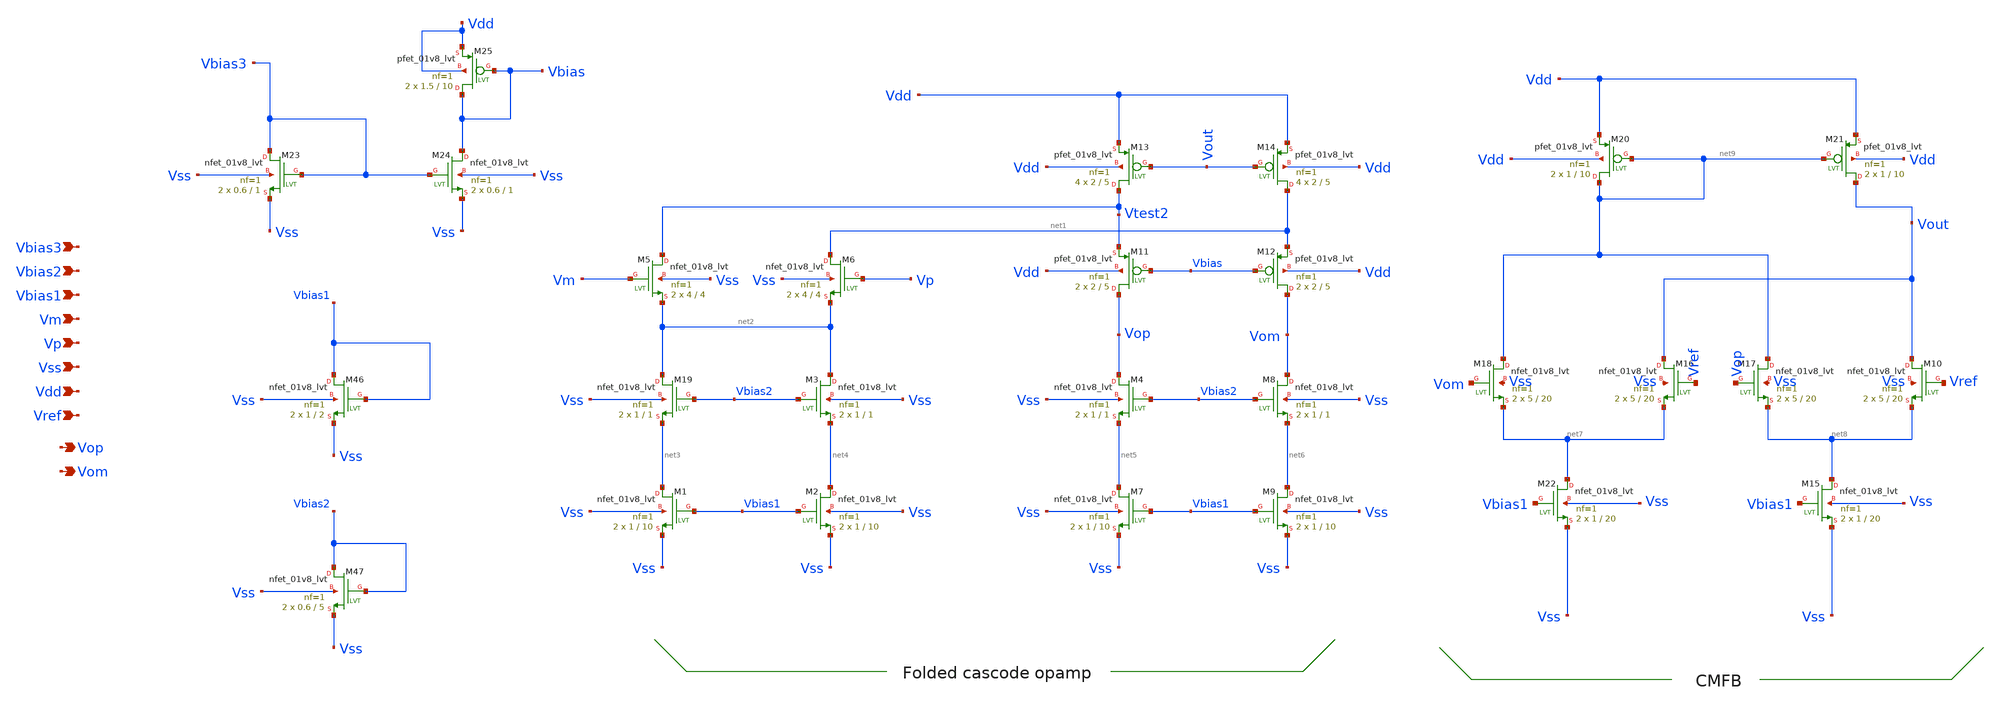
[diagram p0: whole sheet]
** sch_path: src/Opamp_Design/src/Diff_opamp.sch
**.subckt Diff_opamp Vss Vop Vdd Vp Vm Vref Vom Vbias1 Vbias2 Vbias3
*.ipin Vss
*.opin Vop
*.ipin Vdd
*.ipin Vp
*.ipin Vm
*.ipin Vref
*.opin Vom
*.ipin Vbias1
*.ipin Vbias2
*.ipin Vbias3
XM5 Vtest2 Vm net2 Vss sky130_fd_pr__nfet_01v8_lvt L=4 W=4 nf=1 ad='int((nf+1)/2) * W/nf * 0.29' as='int((nf+2)/2) * W/nf * 0.29'
+ pd='2*int((nf+1)/2) * (W/nf + 0.29)' ps='2*int((nf+2)/2) * (W/nf + 0.29)' nrd='0.29 / W' nrs='0.29 / W'
+ sa=0 sb=0 sd=0 mult=2 m=2
XM6 net1 Vp net2 Vss sky130_fd_pr__nfet_01v8_lvt L=4 W=4 nf=1 ad='int((nf+1)/2) * W/nf * 0.29' as='int((nf+2)/2) * W/nf * 0.29'
+ pd='2*int((nf+1)/2) * (W/nf + 0.29)' ps='2*int((nf+2)/2) * (W/nf + 0.29)' nrd='0.29 / W' nrs='0.29 / W'
+ sa=0 sb=0 sd=0 mult=2 m=2
XM11 Vop Vbias Vtest2 Vdd sky130_fd_pr__pfet_01v8_lvt L=5 W=2 nf=1 ad='int((nf+1)/2) * W/nf * 0.29' as='int((nf+2)/2) * W/nf * 0.29'
+ pd='2*int((nf+1)/2) * (W/nf + 0.29)' ps='2*int((nf+2)/2) * (W/nf + 0.29)' nrd='0.29 / W' nrs='0.29 / W'
+ sa=0 sb=0 sd=0 mult=2 m=2
XM12 Vom Vbias net1 Vdd sky130_fd_pr__pfet_01v8_lvt L=5 W=2 nf=1 ad='int((nf+1)/2) * W/nf * 0.29' as='int((nf+2)/2) * W/nf * 0.29'
+ pd='2*int((nf+1)/2) * (W/nf + 0.29)' ps='2*int((nf+2)/2) * (W/nf + 0.29)' nrd='0.29 / W' nrs='0.29 / W'
+ sa=0 sb=0 sd=0 mult=2 m=2
XM13 Vtest2 Vout Vdd Vdd sky130_fd_pr__pfet_01v8_lvt L=5 W=2 nf=1 ad='int((nf+1)/2) * W/nf * 0.29' as='int((nf+2)/2) * W/nf * 0.29'
+ pd='2*int((nf+1)/2) * (W/nf + 0.29)' ps='2*int((nf+2)/2) * (W/nf + 0.29)' nrd='0.29 / W' nrs='0.29 / W'
+ sa=0 sb=0 sd=0 mult=4 m=4
XM14 net1 Vout Vdd Vdd sky130_fd_pr__pfet_01v8_lvt L=5 W=2 nf=1 ad='int((nf+1)/2) * W/nf * 0.29' as='int((nf+2)/2) * W/nf * 0.29'
+ pd='2*int((nf+1)/2) * (W/nf + 0.29)' ps='2*int((nf+2)/2) * (W/nf + 0.29)' nrd='0.29 / W' nrs='0.29 / W'
+ sa=0 sb=0 sd=0 mult=4 m=4
XM19 net2 Vbias2 net3 Vss sky130_fd_pr__nfet_01v8_lvt L=1 W=1 nf=1 ad='int((nf+1)/2) * W/nf * 0.29' as='int((nf+2)/2) * W/nf * 0.29'
+ pd='2*int((nf+1)/2) * (W/nf + 0.29)' ps='2*int((nf+2)/2) * (W/nf + 0.29)' nrd='0.29 / W' nrs='0.29 / W'
+ sa=0 sb=0 sd=0 mult=2 m=2
XM1 net3 Vbias1 Vss Vss sky130_fd_pr__nfet_01v8_lvt L=10 W=1 nf=1 ad='int((nf+1)/2) * W/nf * 0.29' as='int((nf+2)/2) * W/nf * 0.29'
+ pd='2*int((nf+1)/2) * (W/nf + 0.29)' ps='2*int((nf+2)/2) * (W/nf + 0.29)' nrd='0.29 / W' nrs='0.29 / W'
+ sa=0 sb=0 sd=0 mult=2 m=2
XM2 net4 Vbias1 Vss Vss sky130_fd_pr__nfet_01v8_lvt L=10 W=1 nf=1 ad='int((nf+1)/2) * W/nf * 0.29' as='int((nf+2)/2) * W/nf * 0.29'
+ pd='2*int((nf+1)/2) * (W/nf + 0.29)' ps='2*int((nf+2)/2) * (W/nf + 0.29)' nrd='0.29 / W' nrs='0.29 / W'
+ sa=0 sb=0 sd=0 mult=2 m=2
XM3 net2 Vbias2 net4 Vss sky130_fd_pr__nfet_01v8_lvt L=1 W=1 nf=1 ad='int((nf+1)/2) * W/nf * 0.29' as='int((nf+2)/2) * W/nf * 0.29'
+ pd='2*int((nf+1)/2) * (W/nf + 0.29)' ps='2*int((nf+2)/2) * (W/nf + 0.29)' nrd='0.29 / W' nrs='0.29 / W'
+ sa=0 sb=0 sd=0 mult=2 m=2
XM4 Vop Vbias2 net5 Vss sky130_fd_pr__nfet_01v8_lvt L=1 W=1 nf=1 ad='int((nf+1)/2) * W/nf * 0.29' as='int((nf+2)/2) * W/nf * 0.29'
+ pd='2*int((nf+1)/2) * (W/nf + 0.29)' ps='2*int((nf+2)/2) * (W/nf + 0.29)' nrd='0.29 / W' nrs='0.29 / W'
+ sa=0 sb=0 sd=0 mult=2 m=2
XM7 net5 Vbias1 Vss Vss sky130_fd_pr__nfet_01v8_lvt L=10 W=1 nf=1 ad='int((nf+1)/2) * W/nf * 0.29' as='int((nf+2)/2) * W/nf * 0.29'
+ pd='2*int((nf+1)/2) * (W/nf + 0.29)' ps='2*int((nf+2)/2) * (W/nf + 0.29)' nrd='0.29 / W' nrs='0.29 / W'
+ sa=0 sb=0 sd=0 mult=2 m=2
XM8 Vom Vbias2 net6 Vss sky130_fd_pr__nfet_01v8_lvt L=1 W=1 nf=1 ad='int((nf+1)/2) * W/nf * 0.29' as='int((nf+2)/2) * W/nf * 0.29'
+ pd='2*int((nf+1)/2) * (W/nf + 0.29)' ps='2*int((nf+2)/2) * (W/nf + 0.29)' nrd='0.29 / W' nrs='0.29 / W'
+ sa=0 sb=0 sd=0 mult=2 m=2
XM9 net6 Vbias1 Vss Vss sky130_fd_pr__nfet_01v8_lvt L=10 W=1 nf=1 ad='int((nf+1)/2) * W/nf * 0.29' as='int((nf+2)/2) * W/nf * 0.29'
+ pd='2*int((nf+1)/2) * (W/nf + 0.29)' ps='2*int((nf+2)/2) * (W/nf + 0.29)' nrd='0.29 / W' nrs='0.29 / W'
+ sa=0 sb=0 sd=0 mult=2 m=2
XM10 Vout Vref net8 Vss sky130_fd_pr__nfet_01v8_lvt L=20 W=5 nf=1 ad='int((nf+1)/2) * W/nf * 0.29' as='int((nf+2)/2) * W/nf * 0.29'
+ pd='2*int((nf+1)/2) * (W/nf + 0.29)' ps='2*int((nf+2)/2) * (W/nf + 0.29)' nrd='0.29 / W' nrs='0.29 / W'
+ sa=0 sb=0 sd=0 mult=2 m=2
XM17 net9 Vop net8 Vss sky130_fd_pr__nfet_01v8_lvt L=20 W=5 nf=1 ad='int((nf+1)/2) * W/nf * 0.29' as='int((nf+2)/2) * W/nf * 0.29'
+ pd='2*int((nf+1)/2) * (W/nf + 0.29)' ps='2*int((nf+2)/2) * (W/nf + 0.29)' nrd='0.29 / W' nrs='0.29 / W'
+ sa=0 sb=0 sd=0 mult=2 m=2
XM18 net9 Vom net7 Vss sky130_fd_pr__nfet_01v8_lvt L=20 W=5 nf=1 ad='int((nf+1)/2) * W/nf * 0.29' as='int((nf+2)/2) * W/nf * 0.29'
+ pd='2*int((nf+1)/2) * (W/nf + 0.29)' ps='2*int((nf+2)/2) * (W/nf + 0.29)' nrd='0.29 / W' nrs='0.29 / W'
+ sa=0 sb=0 sd=0 mult=2 m=2
XM22 net7 Vbias1 Vss Vss sky130_fd_pr__nfet_01v8_lvt L=20 W=1 nf=1 ad='int((nf+1)/2) * W/nf * 0.29' as='int((nf+2)/2) * W/nf * 0.29'
+ pd='2*int((nf+1)/2) * (W/nf + 0.29)' ps='2*int((nf+2)/2) * (W/nf + 0.29)' nrd='0.29 / W' nrs='0.29 / W'
+ sa=0 sb=0 sd=0 mult=2 m=2
XM20 net9 net9 Vdd Vdd sky130_fd_pr__pfet_01v8_lvt L=10 W=1 nf=1 ad='int((nf+1)/2) * W/nf * 0.29' as='int((nf+2)/2) * W/nf * 0.29'
+ pd='2*int((nf+1)/2) * (W/nf + 0.29)' ps='2*int((nf+2)/2) * (W/nf + 0.29)' nrd='0.29 / W' nrs='0.29 / W'
+ sa=0 sb=0 sd=0 mult=2 m=2
XM21 Vout net9 Vdd Vdd sky130_fd_pr__pfet_01v8_lvt L=10 W=1 nf=1 ad='int((nf+1)/2) * W/nf * 0.29' as='int((nf+2)/2) * W/nf * 0.29'
+ pd='2*int((nf+1)/2) * (W/nf + 0.29)' ps='2*int((nf+2)/2) * (W/nf + 0.29)' nrd='0.29 / W' nrs='0.29 / W'
+ sa=0 sb=0 sd=0 mult=2 m=2
XM15 net8 Vbias1 Vss Vss sky130_fd_pr__nfet_01v8_lvt L=20 W=1 nf=1 ad='int((nf+1)/2) * W/nf * 0.29' as='int((nf+2)/2) * W/nf * 0.29'
+ pd='2*int((nf+1)/2) * (W/nf + 0.29)' ps='2*int((nf+2)/2) * (W/nf + 0.29)' nrd='0.29 / W' nrs='0.29 / W'
+ sa=0 sb=0 sd=0 mult=2 m=2
XM16 Vout Vref net7 Vss sky130_fd_pr__nfet_01v8_lvt L=20 W=5 nf=1 ad='int((nf+1)/2) * W/nf * 0.29' as='int((nf+2)/2) * W/nf * 0.29'
+ pd='2*int((nf+1)/2) * (W/nf + 0.29)' ps='2*int((nf+2)/2) * (W/nf + 0.29)' nrd='0.29 / W' nrs='0.29 / W'
+ sa=0 sb=0 sd=0 mult=2 m=2
XM46 Vbias1 Vbias1 Vss Vss sky130_fd_pr__nfet_01v8_lvt L=2 W=1 nf=1 ad='int((nf+1)/2) * W/nf * 0.29'
+ as='int((nf+2)/2) * W/nf * 0.29' pd='2*int((nf+1)/2) * (W/nf + 0.29)' ps='2*int((nf+2)/2) * (W/nf + 0.29)'
+ nrd='0.29 / W' nrs='0.29 / W' sa=0 sb=0 sd=0 mult=2 m=2
XM47 Vbias2 Vbias2 Vss Vss sky130_fd_pr__nfet_01v8_lvt L=5 W=0.6 nf=1 ad='int((nf+1)/2) * W/nf * 0.29'
+ as='int((nf+2)/2) * W/nf * 0.29' pd='2*int((nf+1)/2) * (W/nf + 0.29)' ps='2*int((nf+2)/2) * (W/nf + 0.29)'
+ nrd='0.29 / W' nrs='0.29 / W' sa=0 sb=0 sd=0 mult=2 m=2
XM23 Vbias3 Vbias3 Vss Vss sky130_fd_pr__nfet_01v8_lvt L=1 W=0.6 nf=1 ad='int((nf+1)/2) * W/nf * 0.29'
+ as='int((nf+2)/2) * W/nf * 0.29' pd='2*int((nf+1)/2) * (W/nf + 0.29)' ps='2*int((nf+2)/2) * (W/nf + 0.29)'
+ nrd='0.29 / W' nrs='0.29 / W' sa=0 sb=0 sd=0 mult=2 m=2
XM24 Vbias Vbias3 Vss Vss sky130_fd_pr__nfet_01v8_lvt L=1 W=0.6 nf=1 ad='int((nf+1)/2) * W/nf * 0.29'
+ as='int((nf+2)/2) * W/nf * 0.29' pd='2*int((nf+1)/2) * (W/nf + 0.29)' ps='2*int((nf+2)/2) * (W/nf + 0.29)'
+ nrd='0.29 / W' nrs='0.29 / W' sa=0 sb=0 sd=0 mult=2 m=2
XM25 Vbias Vbias Vdd Vdd sky130_fd_pr__pfet_01v8_lvt L=10 W=1.5 nf=1 ad='int((nf+1)/2) * W/nf * 0.29'
+ as='int((nf+2)/2) * W/nf * 0.29' pd='2*int((nf+1)/2) * (W/nf + 0.29)' ps='2*int((nf+2)/2) * (W/nf + 0.29)'
+ nrd='0.29 / W' nrs='0.29 / W' sa=0 sb=0 sd=0 mult=2 m=2
**.ends
.end
